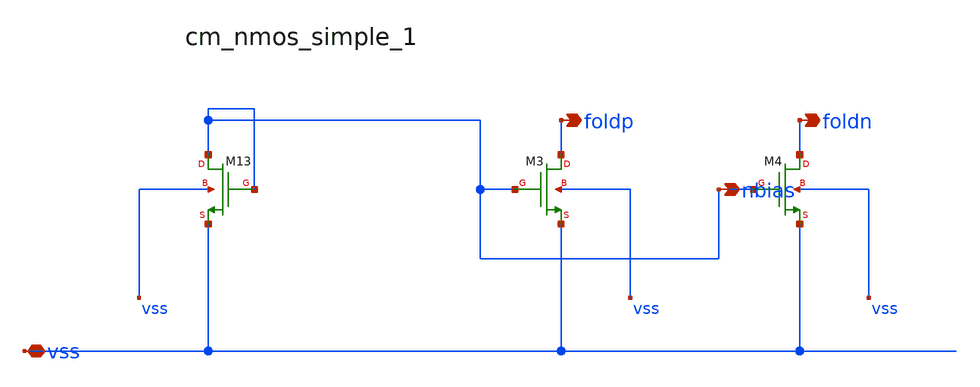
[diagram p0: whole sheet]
** sch_path: analog-db/raw/amp_004_folded_cascode/hier/blocks/cm_nmos_simple_1.sch
**.subckt cm_nmos_simple_1 vss nbias foldp foldn
*.iopin vss
*.opin nbias
*.opin foldp
*.opin foldn
XM13 nbias nbias vss vss sg13_lv_nmos w=x_dut_xm13_w l=x_dut_xm13_l ng=x_dut_xm13_ng m=x_dut_xm13_m
XM3 foldp nbias vss vss sg13_lv_nmos w=x_dut_xm3_w l=x_dut_xm3_l ng=x_dut_xm3_ng m=x_dut_xm3_m
XM4 foldn nbias vss vss sg13_lv_nmos w=x_dut_xm4_w l=x_dut_xm4_l ng=x_dut_xm4_ng m=x_dut_xm4_m
**.ends
.end
